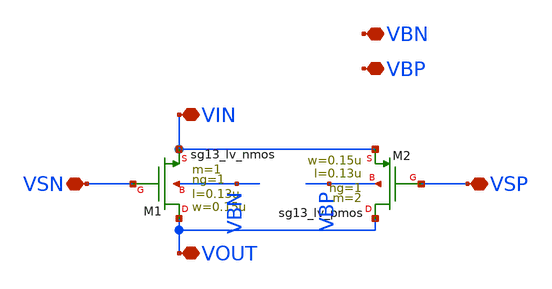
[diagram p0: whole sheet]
** sch_path: PhaseInterpolator/transmission_gate.sch
**.subckt transmission_gate VIN VSN VOUT VSP VBN VBP
*.iopin VIN
*.iopin VSN
*.iopin VOUT
*.iopin VSP
*.iopin VBN
*.iopin VBP
XM1 VOUT VSN VIN VBN sg13_lv_nmos w=0.15u l=0.13u ng=1 m=1 mm_ok=1
XM2 VOUT VSP VIN VBP sg13_lv_pmos w=0.15u l=0.13u ng=1 m=2 mm_ok=1
**.ends
.end
